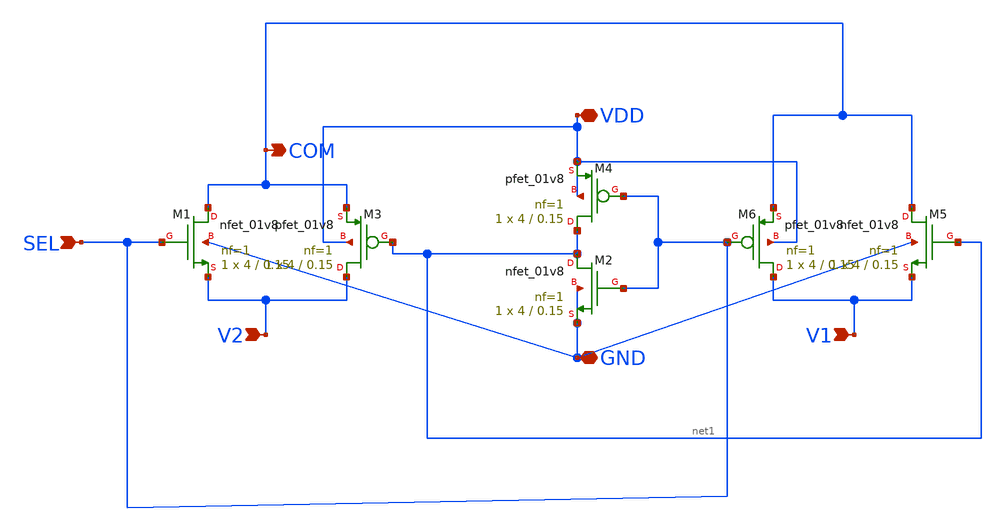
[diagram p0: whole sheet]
** sch_path: SPDT.sch
**.subckt SPDT SEL VDD GND V2 V1 COM
*.ipin SEL
*.iopin VDD
*.iopin GND
*.ipin V2
*.ipin V1
*.opin COM
XM1 COM SEL V2 GND sky130_fd_pr__nfet_01v8 L=0.15 W=4 nf=1 ad='int((1 + 1)/2) * 4 / 1 * 0.29' as='int((1 + 2)/2) * 4 / 1 * 0.29'
+ pd='2*int((1 + 1)/2) * (4 / 1 + 0.29)' ps='2*int((1 + 2)/2) * (4 / 1 + 0.29)' nrd='0.29 / 4 ' nrs='0.29 / 4 '
+ sa=0 sb=0 sd=0 mult=1 m=1
XM2 net1 SEL GND GND sky130_fd_pr__nfet_01v8 L=0.15 W=4 nf=1 ad='int((1 + 1)/2) * 4 / 1 * 0.29' as='int((1 + 2)/2) * 4 / 1 * 0.29'
+ pd='2*int((1 + 1)/2) * (4 / 1 + 0.29)' ps='2*int((1 + 2)/2) * (4 / 1 + 0.29)' nrd='0.29 / 4 ' nrs='0.29 / 4 '
+ sa=0 sb=0 sd=0 mult=1 m=1
XM3 V2 net1 COM VDD sky130_fd_pr__pfet_01v8 L=0.15 W=4 nf=1 ad='int((1 + 1)/2) * 4 / 1 * 0.29' as='int((1 + 2)/2) * 4 / 1 * 0.29'
+ pd='2*int((1 + 1)/2) * (4 / 1 + 0.29)' ps='2*int((1 + 2)/2) * (4 / 1 + 0.29)' nrd='0.29 / 4 ' nrs='0.29 / 4 '
+ sa=0 sb=0 sd=0 mult=1 m=1
XM4 net1 SEL VDD VDD sky130_fd_pr__pfet_01v8 L=0.15 W=4 nf=1 ad='int((1 + 1)/2) * 4 / 1 * 0.29' as='int((1 + 2)/2) * 4 / 1 * 0.29'
+ pd='2*int((1 + 1)/2) * (4 / 1 + 0.29)' ps='2*int((1 + 2)/2) * (4 / 1 + 0.29)' nrd='0.29 / 4 ' nrs='0.29 / 4 '
+ sa=0 sb=0 sd=0 mult=1 m=1
XM5 COM net1 V1 GND sky130_fd_pr__nfet_01v8 L=0.15 W=4 nf=1 ad='int((1 + 1)/2) * 4 / 1 * 0.29' as='int((1 + 2)/2) * 4 / 1 * 0.29'
+ pd='2*int((1 + 1)/2) * (4 / 1 + 0.29)' ps='2*int((1 + 2)/2) * (4 / 1 + 0.29)' nrd='0.29 / 4 ' nrs='0.29 / 4 '
+ sa=0 sb=0 sd=0 mult=1 m=1
XM6 V1 SEL COM VDD sky130_fd_pr__pfet_01v8 L=0.15 W=4 nf=1 ad='int((1 + 1)/2) * 4 / 1 * 0.29' as='int((1 + 2)/2) * 4 / 1 * 0.29'
+ pd='2*int((1 + 1)/2) * (4 / 1 + 0.29)' ps='2*int((1 + 2)/2) * (4 / 1 + 0.29)' nrd='0.29 / 4 ' nrs='0.29 / 4 '
+ sa=0 sb=0 sd=0 mult=1 m=1
**.ends
.end
